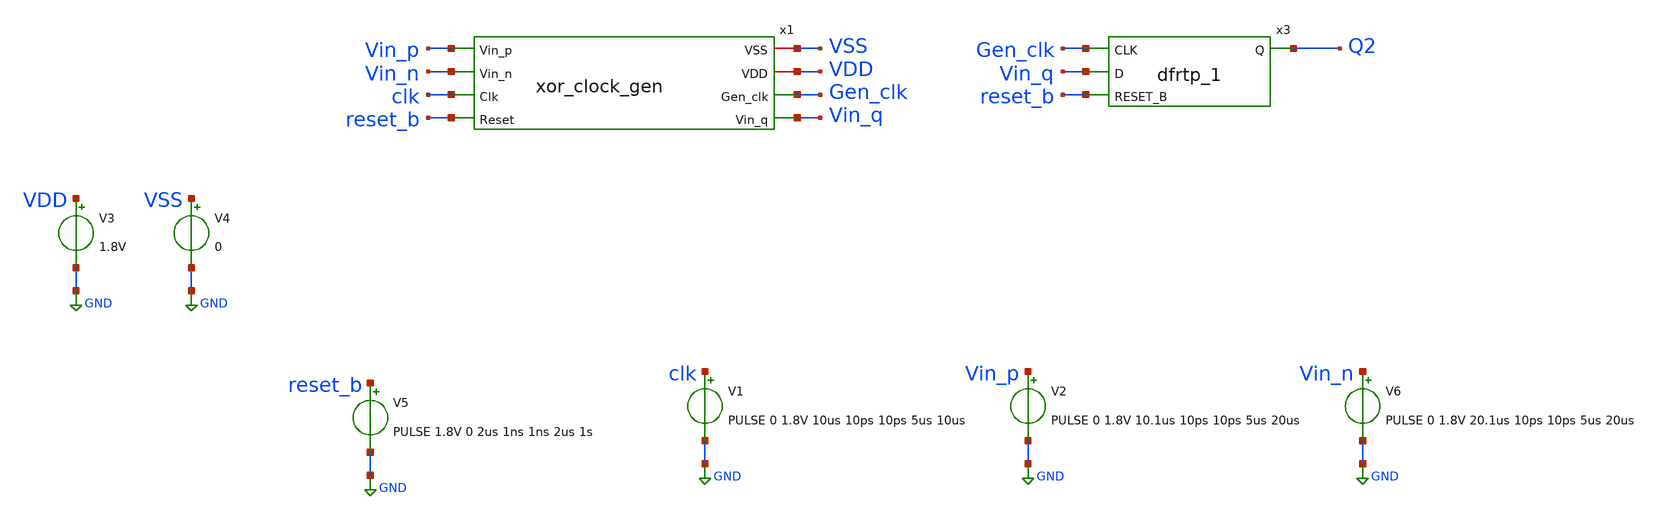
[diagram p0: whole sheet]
** sch_path: xschem/tests/xor_clock_gen/xor_clock_gen_test.sch
**.subckt xor_clock_gen_test
V3 VDD GND 1.8V
V4 VSS GND 0
x1 VSS Vin_p VDD Vin_n Gen_clk clk Vin_q reset_b xor_clock_gen
V5 reset_b GND PULSE 1.8V 0 2us 1ns 1ns 2us 1s
V1 clk GND PULSE 0 1.8V 10us 10ps 10ps 5us 10us
V2 Vin_p GND PULSE 0 1.8V 10.1us 10ps 10ps 5us 20us
V6 Vin_n GND PULSE 0 1.8V 20.1us 10ps 10ps 5us 20us
x3 Gen_clk Vin_q reset_b VSS VSS VDD VDD Q2 sky130_fd_sc_hd__dfrtp_1
**** begin user architecture code
 .lib $::SKYWATER_MODELS/sky130.lib.spice tt
.include $::SKYWATER_STDCELLS/sky130_fd_sc_hd.spice


.options acct list
.temp 25
*vvcc VDD 0 dc 1.8
*vvss VSS 0 0
.control
tran 0.05u 400u
*plot RST_PLS clk+2 Pulse+4
plot Vin_p-Vin_n clk reset_b-2 Gen_clk Vin_q Q2+2
write xor_clock_gen_test.raw
.endc


**** end user architecture code
**.ends

* expanding   symbol:  src/xor_clock_gen/xor_clock_gen.sym # of pins=8
** sym_path: xschem/src/xor_clock_gen/xor_clock_gen.sym
** sch_path: xschem/src/xor_clock_gen/xor_clock_gen.sch
.subckt xor_clock_gen VSS Vin_p VDD Vin_n Gen_clk Clk Vin_q Reset
*.ipin Vin_p
*.iopin VSS
*.opin Gen_clk
*.iopin VDD
*.ipin Vin_n
*.ipin Clk
*.ipin Reset
*.opin Vin_q
x1 Vin_p Vin_n VSS VSS VDD VDD net2 sky130_fd_sc_hd__xor2_1
x14 net24 Vin_p Reset VSS VSS VDD VDD net1 sky130_fd_sc_hd__dfrtp_1
x19 net10 VSS VSS VDD VDD Vin_q sky130_fd_sc_hd__buf_16
x2 net2 VSS VSS VDD VDD net16 sky130_fd_sc_hd__clkdlybuf4s50_1
x3 net3 VSS VSS VDD VDD net4 sky130_fd_sc_hd__clkdlybuf4s50_1
x4 net4 VSS VSS VDD VDD net5 sky130_fd_sc_hd__clkdlybuf4s50_1
x5 net5 VSS VSS VDD VDD net6 sky130_fd_sc_hd__clkdlybuf4s50_1
x6 net6 VSS VSS VDD VDD net7 sky130_fd_sc_hd__clkdlybuf4s50_1
x7 net7 VSS VSS VDD VDD net15 sky130_fd_sc_hd__clkdlybuf4s50_1
x8 net8 VSS VSS VDD VDD Gen_clk sky130_fd_sc_hd__buf_16
x9 net1 VSS VSS VDD VDD net9 sky130_fd_sc_hd__buf_4
x10 net9 VSS VSS VDD VDD net10 sky130_fd_sc_hd__buf_8
x11 net12 VSS VSS VDD VDD net11 sky130_fd_sc_hd__buf_4
x12 net11 VSS VSS VDD VDD net8 sky130_fd_sc_hd__buf_8
XC1 net12 VSS sky130_fd_pr__cap_mim_m3_1 W=25 L=25 MF=1 m=1
x13 net15 VSS VSS VDD VDD net13 sky130_fd_sc_hd__clkdlybuf4s50_1
x15 net13 VSS VSS VDD VDD net14 sky130_fd_sc_hd__clkdlybuf4s50_1
x16 net14 VSS VSS VDD VDD net12 sky130_fd_sc_hd__clkdlybuf4s50_1
x17 net16 VSS VSS VDD VDD net17 sky130_fd_sc_hd__clkdlybuf4s50_1
x18 net17 VSS VSS VDD VDD net18 sky130_fd_sc_hd__clkdlybuf4s50_1
x20 net18 VSS VSS VDD VDD net19 sky130_fd_sc_hd__clkdlybuf4s50_1
x21 net19 VSS VSS VDD VDD net20 sky130_fd_sc_hd__clkdlybuf4s50_1
x22 net20 VSS VSS VDD VDD net23 sky130_fd_sc_hd__clkdlybuf4s50_1
x23 net23 VSS VSS VDD VDD net21 sky130_fd_sc_hd__clkdlybuf4s50_1
x24 net21 VSS VSS VDD VDD net22 sky130_fd_sc_hd__clkdlybuf4s50_1
x25 net22 VSS VSS VDD VDD net3 sky130_fd_sc_hd__clkdlybuf4s50_1
x26 net20 VSS VSS VDD VDD net24 sky130_fd_sc_hd__buf_1
.ends

.GLOBAL GND
.end
